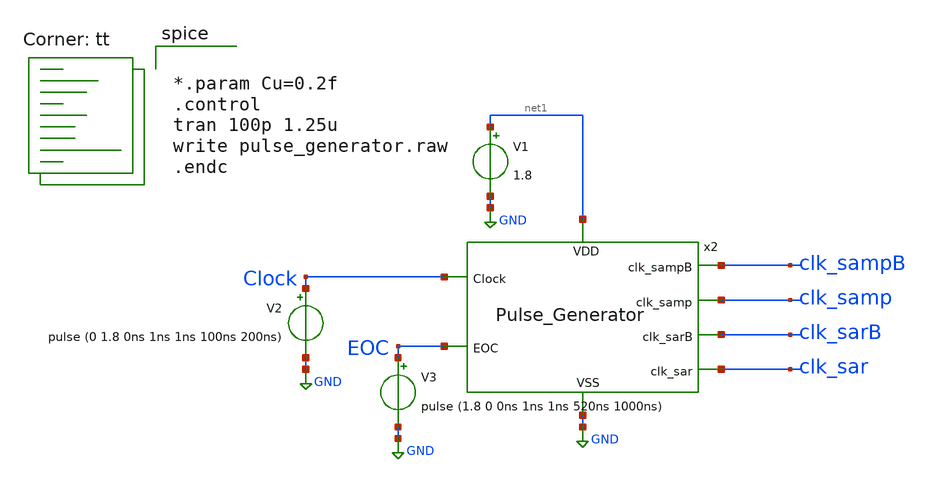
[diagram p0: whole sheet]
** sch_path: Pulse_Generator_tb.sch
**.subckt Pulse_Generator_tb
V1 net1 GND 1.8
V2 Clock GND pulse (0 1.8 0ns 1ns 1ns 100ns 200ns)
V3 EOC GND pulse (1.8 0 0ns 1ns 1ns 520ns 1000ns)
x2 net1 Clock clk_sampB clk_samp clk_sarB EOC clk_sar GND Pulse_Generator
**** begin user architecture code
.lib $::SKYWATER_MODELS/sky130.lib.spice tt


*.param Cu=0.2f
.control
tran 100p 1.25u
write pulse_generator.raw
.endc


**** end user architecture code
**.ends
.GLOBAL GND
.end
